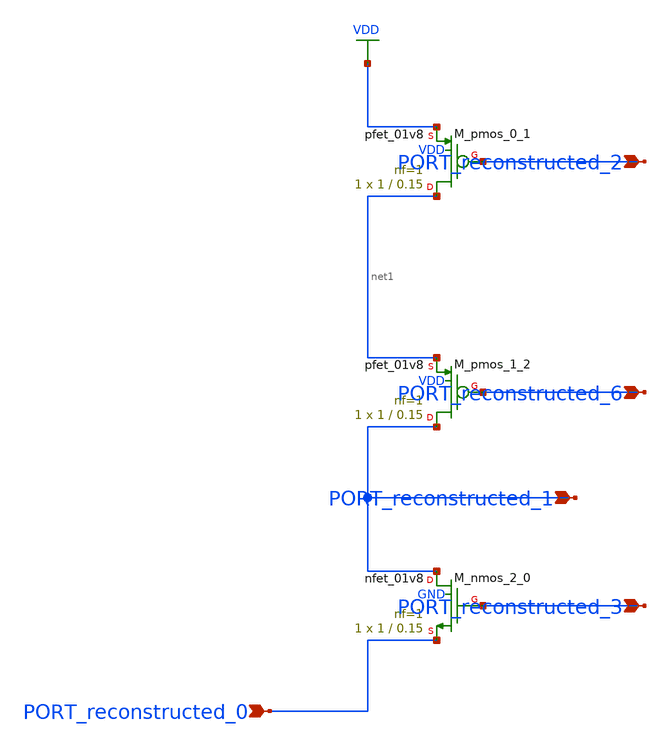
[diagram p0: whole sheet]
** sch_path: schematics/AMSNet/173.sch
**.subckt 173 PORT_reconstructed_6 PORT_reconstructed_2 PORT_reconstructed_3 PORT_reconstructed_1
*+ PORT_reconstructed_0
*.ipin PORT_reconstructed_6
*.ipin PORT_reconstructed_2
*.ipin PORT_reconstructed_3
*.ipin PORT_reconstructed_1
*.ipin PORT_reconstructed_0
XM_nmos_2_0 PORT_reconstructed_1 PORT_reconstructed_3 PORT_reconstructed_0 GND sky130_fd_pr__nfet_01v8
+ L=0.15 W=1 nf=1 ad='int((1 + 1)/2) * 1 / 1 * 0.29' as='int((1 + 2)/2) * 1 / 1 * 0.29' pd='2*int((1 + 1)/2) * (1 / 1 + 0.29)'
+ ps='2*int((1 + 2)/2) * (1 / 1 + 0.29)' nrd='0.29 / 1 ' nrs='0.29 / 1 ' sa=0 sb=0 sd=0 mult=1 m=1
XM_pmos_0_1 net1 PORT_reconstructed_2 VDD VDD sky130_fd_pr__pfet_01v8 L=0.15 W=1 nf=1 ad='int((1 + 1)/2) * 1 / 1 * 0.29'
+ as='int((1 + 2)/2) * 1 / 1 * 0.29' pd='2*int((1 + 1)/2) * (1 / 1 + 0.29)' ps='2*int((1 + 2)/2) * (1 / 1 + 0.29)'
+ nrd='0.29 / 1 ' nrs='0.29 / 1 ' sa=0 sb=0 sd=0 mult=1 m=1
XM_pmos_1_2 PORT_reconstructed_1 PORT_reconstructed_6 net1 VDD sky130_fd_pr__pfet_01v8 L=0.15 W=1 nf=1
+ ad='int((1 + 1)/2) * 1 / 1 * 0.29' as='int((1 + 2)/2) * 1 / 1 * 0.29' pd='2*int((1 + 1)/2) * (1 / 1 + 0.29)'
+ ps='2*int((1 + 2)/2) * (1 / 1 + 0.29)' nrd='0.29 / 1 ' nrs='0.29 / 1 ' sa=0 sb=0 sd=0 mult=1 m=1
**.ends
.GLOBAL VDD
.end
